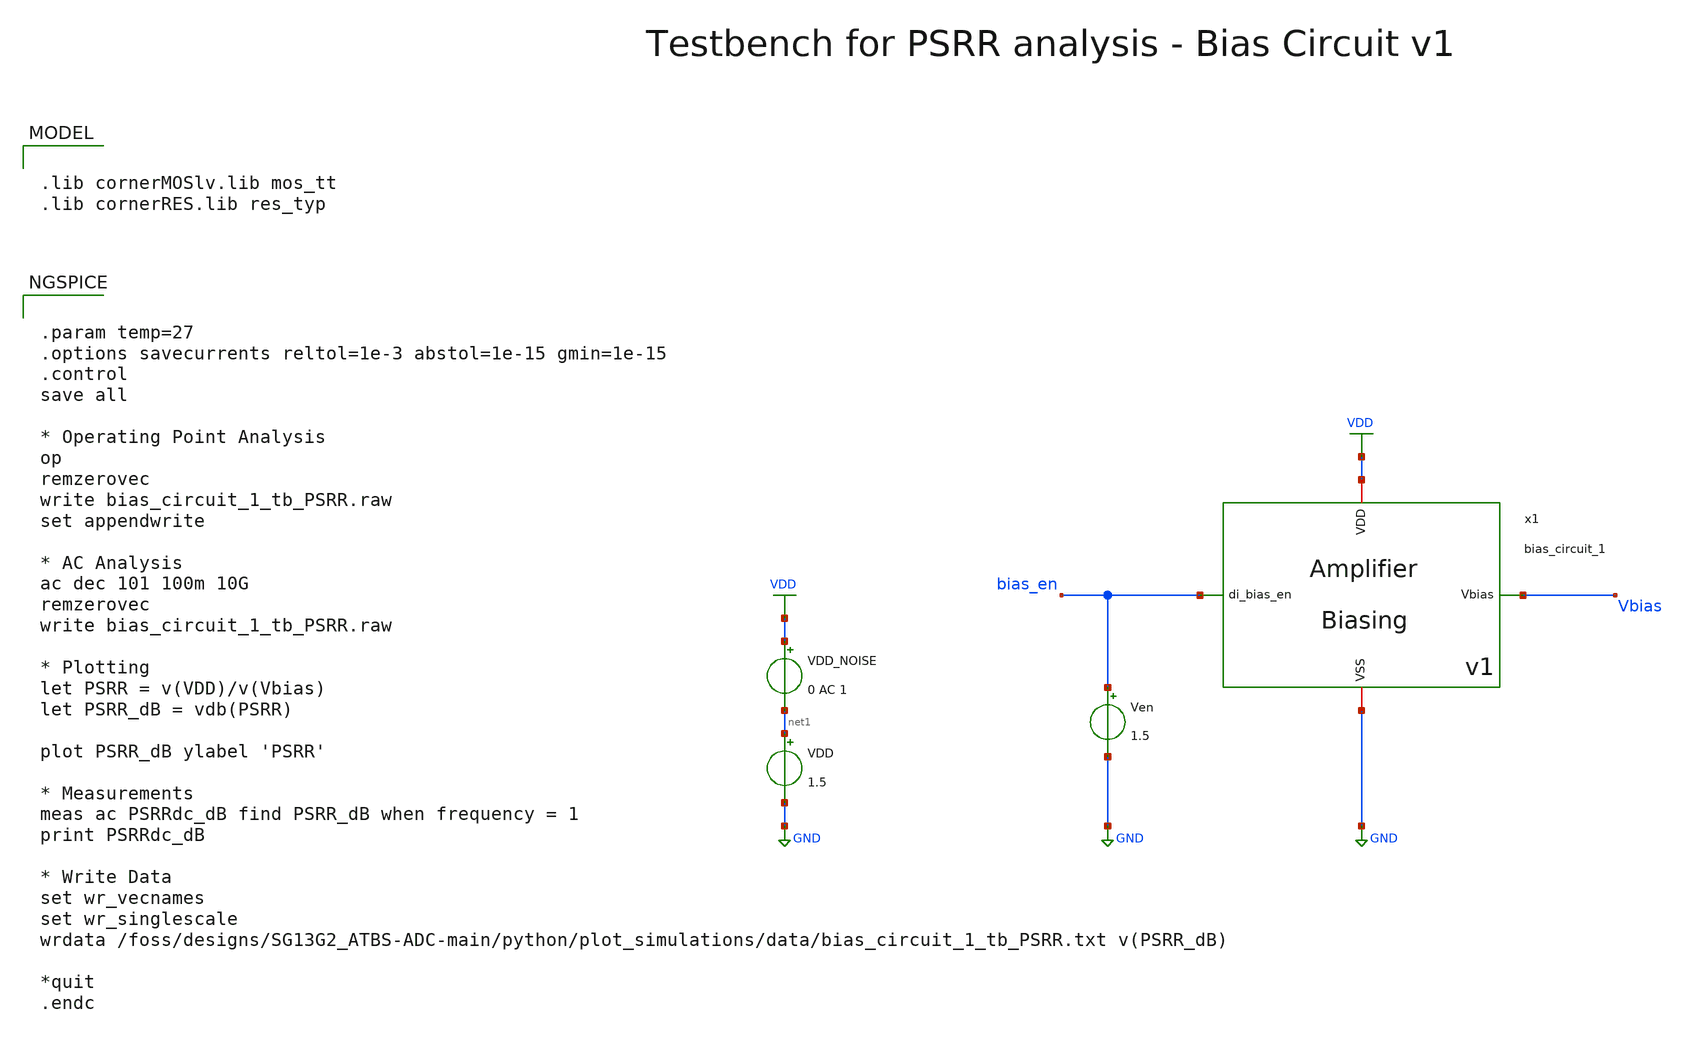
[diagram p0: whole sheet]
** sch_path: SG13G2_ATBS-ADC-main/xschem/bio_amplifier/amplifier_core/bias_circuit/bias_circuit_1/testbenches/bias_circuit_1_tb_PSRR.sch
**.subckt bias_circuit_1_tb_PSRR
Ven bias_en GND 1.5
VDD net1 GND 1.5
x1 bias_en Vbias VDD GND bias_circuit_1
VDD_NOISE VDD net1 0 AC 1
**** begin user architecture code

.lib cornerMOSlv.lib mos_tt
.lib cornerRES.lib res_typ



.param temp=27
.options savecurrents reltol=1e-3 abstol=1e-15 gmin=1e-15
.control
save all

* Operating Point Analysis
op
remzerovec
write bias_circuit_1_tb_PSRR.raw
set appendwrite

* AC Analysis
ac dec 101 100m 10G
remzerovec
write bias_circuit_1_tb_PSRR.raw

* Plotting
let PSRR = v(VDD)/v(Vbias)
let PSRR_dB = vdb(PSRR)

plot PSRR_dB ylabel 'PSRR'

* Measurements
meas ac PSRRdc_dB find PSRR_dB when frequency = 1
print PSRRdc_dB

* Write Data
set wr_vecnames
set wr_singlescale
wrdata /foss/designs/SG13G2_ATBS-ADC-main/python/plot_simulations/data/bias_circuit_1_tb_PSRR.txt
+ v(PSRR_dB)

*quit
.endc

**** end user architecture code
**.ends
.GLOBAL GND
.GLOBAL VDD
.end
